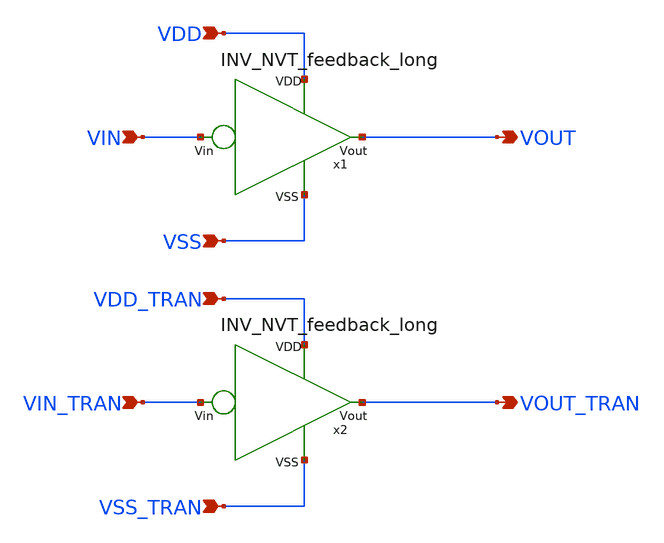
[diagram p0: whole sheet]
** sch_path: design/THESIS_EXP_RO_INVERTER_SKY130A/TB_Cout_NVT_L.sch
**.subckt TB_Cout_NVT_L VOUT VIN VSS VDD VDD_TRAN VIN_TRAN VSS_TRAN VOUT_TRAN
*.opin VOUT
*.ipin VIN
*.ipin VSS
*.ipin VDD
*.ipin VDD_TRAN
*.ipin VIN_TRAN
*.ipin VSS_TRAN
*.opin VOUT_TRAN
x1 VDD VSS VOUT VIN INV_NVT_feedback_long
x2 VDD_TRAN VSS_TRAN VOUT_TRAN VIN_TRAN INV_NVT_feedback_long
**.ends

* expanding   symbol:  THESIS_EXP_RO_INVERTER_SKY130A/INV_NVT_feedback_long.sym # of pins=4
** sym_path: design/THESIS_EXP_RO_INVERTER_SKY130A/INV_NVT_feedback_long.sym
** sch_path: design/THESIS_EXP_RO_INVERTER_SKY130A/INV_NVT_feedback_long.sch
.subckt INV_NVT_feedback_long VDD VSS Vout Vin
*.ipin VSS
*.ipin Vin
*.opin Vout
*.ipin VDD
XM1 Vout Vin VDD VDD sky130_fd_pr__pfet_01v8_lvt L=0.35 W=7 nf=1 ad='int((nf+1)/2) * W/nf * 0.29' as='int((nf+2)/2) * W/nf * 0.29'
+ pd='2*int((nf+1)/2) * (W/nf + 0.29)' ps='2*int((nf+2)/2) * (W/nf + 0.29)' nrd='0.29 / W' nrs='0.29 / W'
+ sa=0 sb=0 sd=0 mult=m_alpha m=m_alpha
XM2 Vout Vin vn VSS sky130_fd_pr__nfet_03v3_nvt L=0.8 W=0.42 nf=1 ad='int((nf+1)/2) * W/nf * 0.29' as='int((nf+2)/2) * W/nf * 0.29'
+ pd='2*int((nf+1)/2) * (W/nf + 0.29)' ps='2*int((nf+2)/2) * (W/nf + 0.29)' nrd='0.29 / W' nrs='0.29 / W'
+ sa=0 sb=0 sd=0 mult=m_beta m=m_beta
XM3 vn Vin VSS VSS sky130_fd_pr__nfet_03v3_nvt L=0.8 W=0.42 nf=1 ad='int((nf+1)/2) * W/nf * 0.29' as='int((nf+2)/2) * W/nf * 0.29'
+ pd='2*int((nf+1)/2) * (W/nf + 0.29)' ps='2*int((nf+2)/2) * (W/nf + 0.29)' nrd='0.29 / W' nrs='0.29 / W'
+ sa=0 sb=0 sd=0 mult=m_I0 m=m_I0
XM4 VDD Vout vn VSS sky130_fd_pr__nfet_03v3_nvt L=0.8 W=0.42 nf=1 ad='int((nf+1)/2) * W/nf * 0.29' as='int((nf+2)/2) * W/nf * 0.29'
+ pd='2*int((nf+1)/2) * (W/nf + 0.29)' ps='2*int((nf+2)/2) * (W/nf + 0.29)' nrd='0.29 / W' nrs='0.29 / W'
+ sa=0 sb=0 sd=0 mult=m_gamma m=m_gamma
.ends

.end
